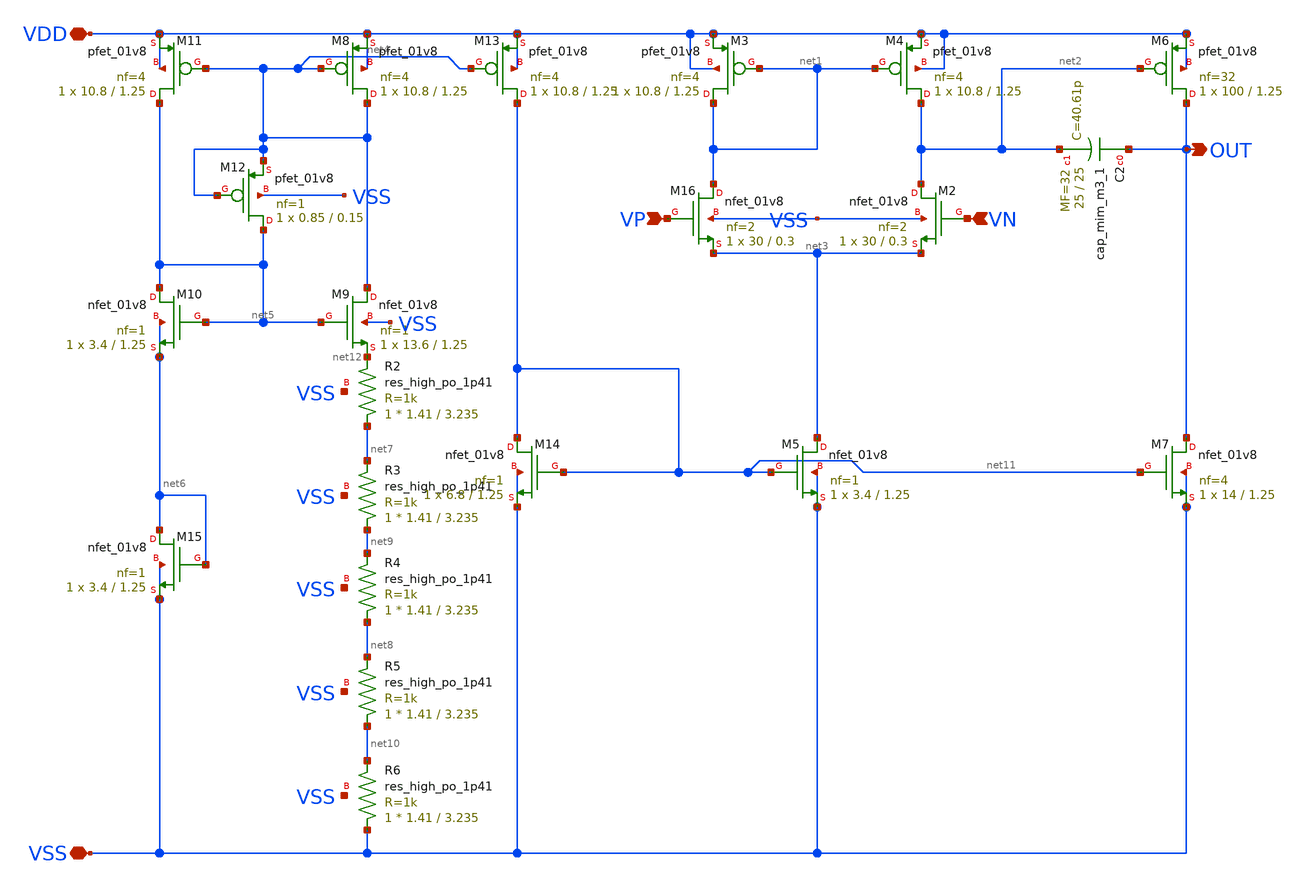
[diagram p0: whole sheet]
** sch_path: bandgap/bgr-opamp/bgr-opamp.sch
**.subckt bgr-opamp VSS VDD VP VN OUT
*.iopin VSS
*.iopin VDD
*.ipin VP
*.ipin VN
*.opin OUT
XM2 net2 VN net3 VSS sky130_fd_pr__nfet_01v8 L=0.3 W=30 nf=2 ad='int((nf+1)/2) * W/nf * 0.29' as='int((nf+2)/2) * W/nf * 0.29'
+ pd='2*int((nf+1)/2) * (W/nf + 0.29)' ps='2*int((nf+2)/2) * (W/nf + 0.29)' nrd='0.29 / W' nrs='0.29 / W'
+ sa=0 sb=0 sd=0 mult=1 m=1
XM4 net2 net1 VDD VDD sky130_fd_pr__pfet_01v8 L=1.25 W=10.8 nf=4 ad='int((nf+1)/2) * W/nf * 0.29' as='int((nf+2)/2) * W/nf * 0.29'
+ pd='2*int((nf+1)/2) * (W/nf + 0.29)' ps='2*int((nf+2)/2) * (W/nf + 0.29)' nrd='0.29 / W' nrs='0.29 / W'
+ sa=0 sb=0 sd=0 mult=1 m=1
XM3 net1 net1 VDD VDD sky130_fd_pr__pfet_01v8 L=1.25 W=10.8 nf=4 ad='int((nf+1)/2) * W/nf * 0.29' as='int((nf+2)/2) * W/nf * 0.29'
+ pd='2*int((nf+1)/2) * (W/nf + 0.29)' ps='2*int((nf+2)/2) * (W/nf + 0.29)' nrd='0.29 / W' nrs='0.29 / W'
+ sa=0 sb=0 sd=0 mult=1 m=1
XM5 net3 net11 VSS VSS sky130_fd_pr__nfet_01v8 L=1.25 W=3.4 nf=1 ad='int((nf+1)/2) * W/nf * 0.29' as='int((nf+2)/2) * W/nf * 0.29'
+ pd='2*int((nf+1)/2) * (W/nf + 0.29)' ps='2*int((nf+2)/2) * (W/nf + 0.29)' nrd='0.29 / W' nrs='0.29 / W'
+ sa=0 sb=0 sd=0 mult=1 m=1
XM9 net4 net5 net12 VSS sky130_fd_pr__nfet_01v8 L=1.25 W=13.6 nf=1 ad='int((nf+1)/2) * W/nf * 0.29' as='int((nf+2)/2) * W/nf * 0.29'
+ pd='2*int((nf+1)/2) * (W/nf + 0.29)' ps='2*int((nf+2)/2) * (W/nf + 0.29)' nrd='0.29 / W' nrs='0.29 / W'
+ sa=0 sb=0 sd=0 mult=1 m=1
XM8 net4 net4 VDD VDD sky130_fd_pr__pfet_01v8 L=1.25 W=10.8 nf=4 ad='int((nf+1)/2) * W/nf * 0.29' as='int((nf+2)/2) * W/nf * 0.29'
+ pd='2*int((nf+1)/2) * (W/nf + 0.29)' ps='2*int((nf+2)/2) * (W/nf + 0.29)' nrd='0.29 / W' nrs='0.29 / W'
+ sa=0 sb=0 sd=0 mult=1 m=1
XM11 net5 net4 VDD VDD sky130_fd_pr__pfet_01v8 L=1.25 W=10.8 nf=4 ad='int((nf+1)/2) * W/nf * 0.29' as='int((nf+2)/2) * W/nf * 0.29'
+ pd='2*int((nf+1)/2) * (W/nf + 0.29)' ps='2*int((nf+2)/2) * (W/nf + 0.29)' nrd='0.29 / W' nrs='0.29 / W'
+ sa=0 sb=0 sd=0 mult=1 m=1
XM10 net5 net5 net6 net6 sky130_fd_pr__nfet_01v8 L=1.25 W=3.4 nf=1 ad='int((nf+1)/2) * W/nf * 0.29' as='int((nf+2)/2) * W/nf * 0.29'
+ pd='2*int((nf+1)/2) * (W/nf + 0.29)' ps='2*int((nf+2)/2) * (W/nf + 0.29)' nrd='0.29 / W' nrs='0.29 / W'
+ sa=0 sb=0 sd=0 mult=1 m=1
XM6 OUT net2 VDD VDD sky130_fd_pr__pfet_01v8 L=1.25 W=100 nf=32 ad='int((nf+1)/2) * W/nf * 0.29' as='int((nf+2)/2) * W/nf * 0.29'
+ pd='2*int((nf+1)/2) * (W/nf + 0.29)' ps='2*int((nf+2)/2) * (W/nf + 0.29)' nrd='0.29 / W' nrs='0.29 / W'
+ sa=0 sb=0 sd=0 mult=1 m=1
XM7 OUT net11 VSS VSS sky130_fd_pr__nfet_01v8 L=1.25 W=14 nf=4 ad='int((nf+1)/2) * W/nf * 0.29' as='int((nf+2)/2) * W/nf * 0.29'
+ pd='2*int((nf+1)/2) * (W/nf + 0.29)' ps='2*int((nf+2)/2) * (W/nf + 0.29)' nrd='0.29 / W' nrs='0.29 / W'
+ sa=0 sb=0 sd=0 mult=1 m=1
XC2 OUT net2 sky130_fd_pr__cap_mim_m3_1 W=25 L=25 MF=32 m=32
XR2 net7 net12 VSS sky130_fd_pr__res_high_po_1p41 L=3.235 mult=1 m=1
XR3 net9 net7 VSS sky130_fd_pr__res_high_po_1p41 L=3.235 mult=1 m=1
XR4 net8 net9 VSS sky130_fd_pr__res_high_po_1p41 L=3.235 mult=1 m=1
XR5 net10 net8 VSS sky130_fd_pr__res_high_po_1p41 L=3.235 mult=1 m=1
XR6 VSS net10 VSS sky130_fd_pr__res_high_po_1p41 L=3.235 mult=1 m=1
XM13 net11 net4 VDD VDD sky130_fd_pr__pfet_01v8 L=1.25 W=10.8 nf=4 ad='int((nf+1)/2) * W/nf * 0.29' as='int((nf+2)/2) * W/nf * 0.29'
+ pd='2*int((nf+1)/2) * (W/nf + 0.29)' ps='2*int((nf+2)/2) * (W/nf + 0.29)' nrd='0.29 / W' nrs='0.29 / W'
+ sa=0 sb=0 sd=0 mult=1 m=1
XM14 net11 net11 VSS VSS sky130_fd_pr__nfet_01v8 L=1.25 W=6.8 nf=1 ad='int((nf+1)/2) * W/nf * 0.29' as='int((nf+2)/2) * W/nf * 0.29'
+ pd='2*int((nf+1)/2) * (W/nf + 0.29)' ps='2*int((nf+2)/2) * (W/nf + 0.29)' nrd='0.29 / W' nrs='0.29 / W'
+ sa=0 sb=0 sd=0 mult=1 m=1
XM15 net6 net6 VSS VSS sky130_fd_pr__nfet_01v8 L=1.25 W=3.4 nf=1 ad='int((nf+1)/2) * W/nf * 0.29' as='int((nf+2)/2) * W/nf * 0.29'
+ pd='2*int((nf+1)/2) * (W/nf + 0.29)' ps='2*int((nf+2)/2) * (W/nf + 0.29)' nrd='0.29 / W' nrs='0.29 / W'
+ sa=0 sb=0 sd=0 mult=1 m=1
XM12 net5 net4 net4 VSS sky130_fd_pr__pfet_01v8 L=0.15 W=0.85 nf=1 ad='int((nf+1)/2) * W/nf * 0.29' as='int((nf+2)/2) * W/nf * 0.29'
+ pd='2*int((nf+1)/2) * (W/nf + 0.29)' ps='2*int((nf+2)/2) * (W/nf + 0.29)' nrd='0.29 / W' nrs='0.29 / W'
+ sa=0 sb=0 sd=0 mult=1 m=1
XM16 net1 VP net3 VSS sky130_fd_pr__nfet_01v8 L=0.3 W=30 nf=2 ad='int((nf+1)/2) * W/nf * 0.29' as='int((nf+2)/2) * W/nf * 0.29'
+ pd='2*int((nf+1)/2) * (W/nf + 0.29)' ps='2*int((nf+2)/2) * (W/nf + 0.29)' nrd='0.29 / W' nrs='0.29 / W'
+ sa=0 sb=0 sd=0 mult=1 m=1
**.ends
.end
